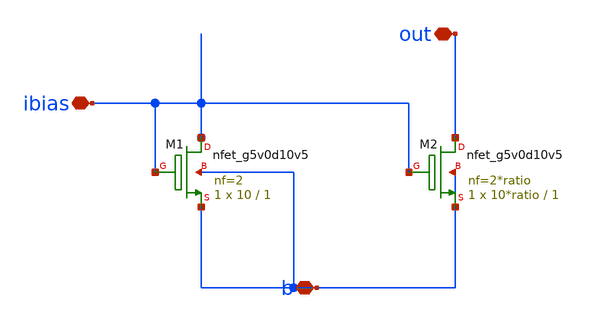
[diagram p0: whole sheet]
** sch_path: xschem/mosbius_lib/mosbius_nsink.sch
**.subckt mosbius_nsink ibias b out
*.iopin ibias
*.iopin b
*.iopin out
XM1 ibias ibias b b sky130_fd_pr__nfet_g5v0d10v5 L=1 W=10 nf=2 ad='int((nf+1)/2) * W/nf * 0.29' as='int((nf+2)/2) * W/nf * 0.29'
+ pd='2*int((nf+1)/2) * (W/nf + 0.29)' ps='2*int((nf+2)/2) * (W/nf + 0.29)' nrd='0.29 / W' nrs='0.29 / W'
+ sa=0 sb=0 sd=0 mult=1 m=1
XM2 out ibias b b sky130_fd_pr__nfet_g5v0d10v5 L=1 W=10*ratio nf=2*ratio ad='int((nf+1)/2) * W/nf * 0.29'
+ as='int((nf+2)/2) * W/nf * 0.29' pd='2*int((nf+1)/2) * (W/nf + 0.29)' ps='2*int((nf+2)/2) * (W/nf + 0.29)'
+ nrd='0.29 / W' nrs='0.29 / W' sa=0 sb=0 sd=0 mult=1 m=1
**.ends
.end
